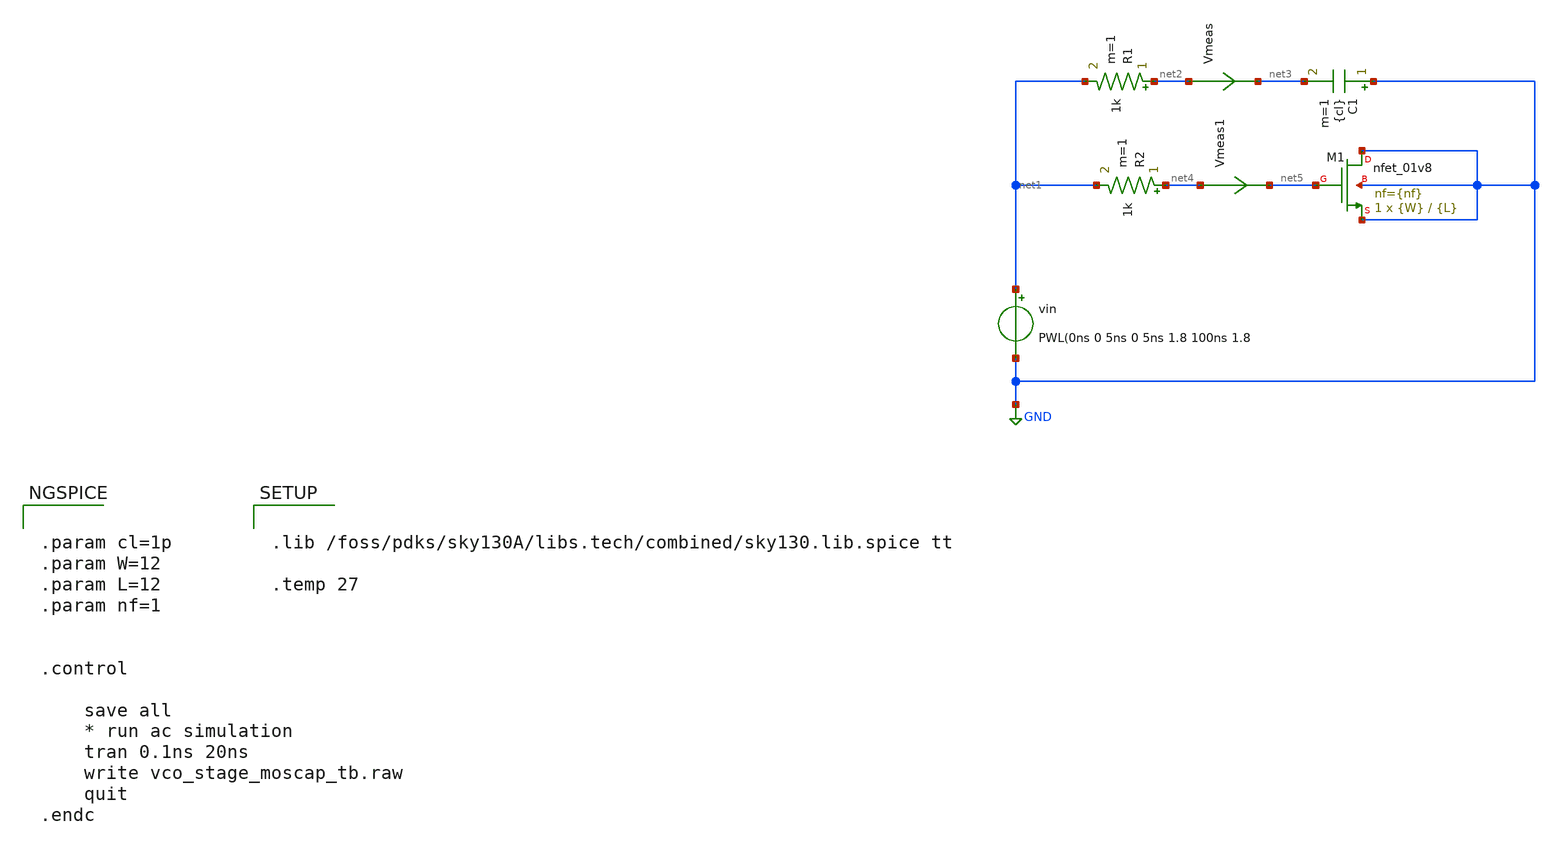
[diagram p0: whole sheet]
** sch_path: xschem/vco_stage_moscap_tb.sch
**.subckt vco_stage_moscap_tb
vin net1 GND PWL(0ns 0 5ns 0 5ns 1.8 100ns 1.8
R1 net2 net1 1k m=1
C1 GND net3 {cl} m=1
Vmeas net2 net3 0
.save i(vmeas)
XM1 GND net5 GND GND sky130_fd_pr__nfet_01v8 L={L} W={W} nf={nf} ad='int((nf+1)/2) * W/nf * 0.29' as='int((nf+2)/2) * W/nf * 0.29'
+ pd='2*int((nf+1)/2) * (W/nf + 0.29)' ps='2*int((nf+2)/2) * (W/nf + 0.29)' nrd='0.29 / W' nrs='0.29 / W'
+ sa=0 sb=0 sd=0 mult=1 m=1
R2 net4 net1 1k m=1
Vmeas1 net4 net5 0
.save i(vmeas1)
**** begin user architecture code


.param cl=1p
.param W=12
.param L=12
.param nf=1


.control

    save all
    * run ac simulation
    tran 0.1ns 20ns
    write vco_stage_moscap_tb.raw
    quit
.endc




.lib /foss/pdks/sky130A/libs.tech/combined/sky130.lib.spice tt

.temp 27


**** end user architecture code
**.ends
.GLOBAL GND
.end
